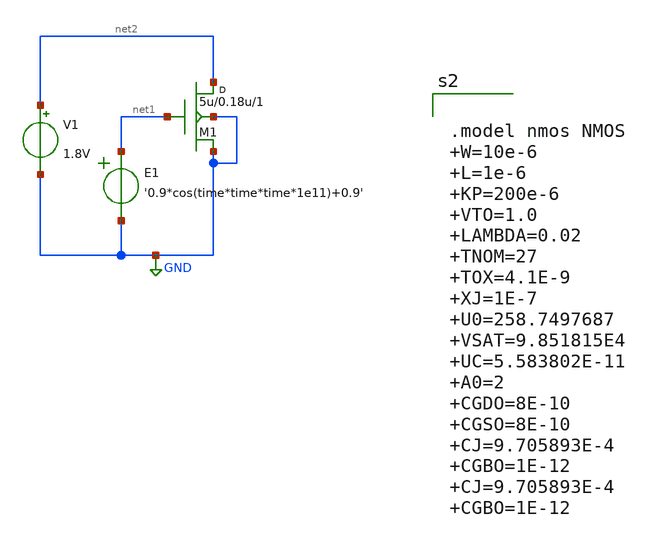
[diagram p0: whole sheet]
** sch_path: Day1/inverter/xschem/inverter_tb1.sch
**.subckt inverter_tb1
V1 net2 GND 1.8V
E1 net1 GND VOL=' '0.9*cos(time*time*time*1e11)+0.9' '
M1 net2 net1 GND GND nmos w=5u l=0.18u m=1
**** begin user architecture code

.tran 1n 2u



.model nmos NMOS  W=10e-6  L=1e-6  KP=200e-6  VTO=1.0  LAMBDA=0.02  TNOM=27  TOX=4.1E-9  XJ=1E-7
+  U0=258.7497687  VSAT=9.851815E4  UC=5.583802E-11  A0=2  CGDO=8E-10  CGSO=8E-10  CJ=9.705893E-4  CGBO=1E-12
+  CJ=9.705893E-4  CGBO=1E-12


**** end user architecture code
**.ends
.GLOBAL GND
.end
